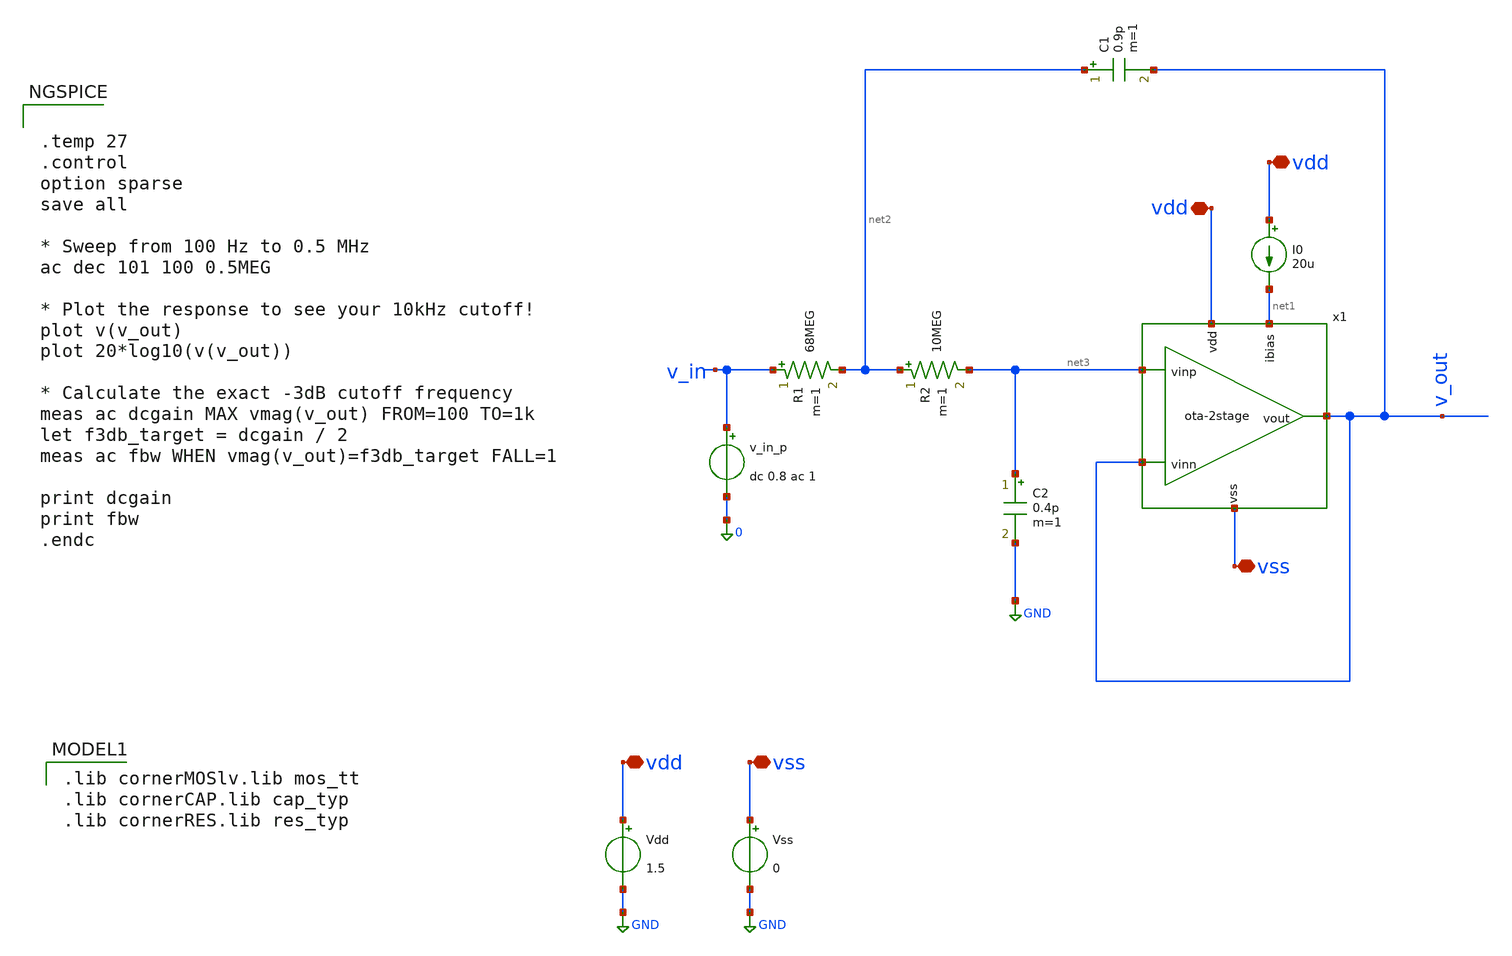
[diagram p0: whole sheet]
** sch_path: xschem/ota-2stage_tb-sk-lpf.sch
**.subckt ota-2stage_tb-sk-lpf vdd vdd vdd vss vss
*.iopin vdd
*.iopin vdd
*.iopin vdd
*.iopin vss
*.iopin vss
I0 vdd net1 20u
Vdd vdd GND 1.5
Vss vss GND 0
v_in_p v_in 0 dc 0.8 ac 1
R1 v_in net2 68MEG m=1
R2 net2 net3 10MEG m=1
C2 net3 GND 0.4p m=1
C1 net2 v_out 0.9p m=1
x1 vdd net1 v_out v_out net3 vss ota-2stage
**** begin user architecture code


.temp 27
.control
option sparse
save all

* Sweep from 100 Hz to 0.5 MHz
ac dec 101 100 0.5MEG

* Plot the response to see your 10kHz cutoff!
plot v(v_out)
plot 20*log10(v(v_out))

* Calculate the exact -3dB cutoff frequency
meas ac dcgain MAX vmag(v_out) FROM=100 TO=1k
let f3db_target = dcgain / 2
meas ac fbw WHEN vmag(v_out)=f3db_target FALL=1

print dcgain
print fbw
.endc


 .lib cornerMOSlv.lib mos_tt
.lib cornerCAP.lib cap_typ
.lib cornerRES.lib res_typ

**** end user architecture code
**.ends
.GLOBAL GND
.end
